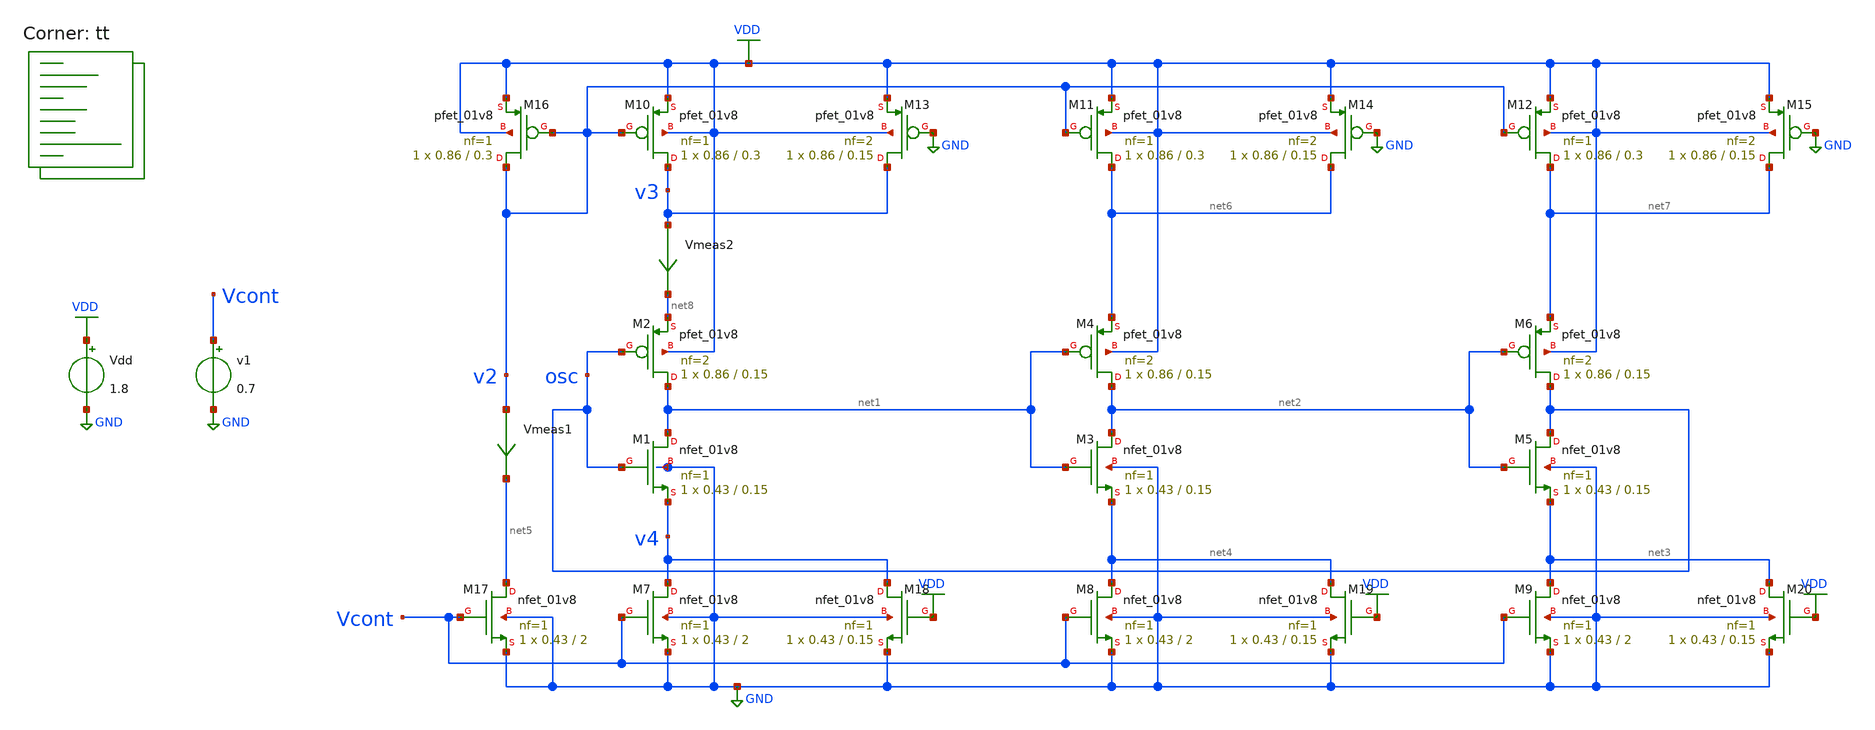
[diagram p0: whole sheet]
** sch_path: projects/pll/vco/xschem_ngspice/tb_current_starved_VCO4_4.sch
**.subckt tb_current_starved_VCO4_4
Vdd VDD GND 1.8
v1 Vcont GND 0.7
XM1 net1 osc v4 GND sky130_fd_pr__nfet_01v8 L=0.15 W=0.43 nf=1 ad='int((nf+1)/2) * W/nf * 0.29' as='int((nf+2)/2) * W/nf * 0.29'
+ pd='2*int((nf+1)/2) * (W/nf + 0.29)' ps='2*int((nf+2)/2) * (W/nf + 0.29)' nrd='0.29 / W' nrs='0.29 / W'
+ sa=0 sb=0 sd=0 mult=1 m=1
XM2 net1 osc net8 VDD sky130_fd_pr__pfet_01v8 L=0.15 W=0.86 nf=2 ad='int((nf+1)/2) * W/nf * 0.29' as='int((nf+2)/2) * W/nf * 0.29'
+ pd='2*int((nf+1)/2) * (W/nf + 0.29)' ps='2*int((nf+2)/2) * (W/nf + 0.29)' nrd='0.29 / W' nrs='0.29 / W'
+ sa=0 sb=0 sd=0 mult=1 m=1
XM3 net2 net1 net4 GND sky130_fd_pr__nfet_01v8 L=0.15 W=0.43 nf=1 ad='int((nf+1)/2) * W/nf * 0.29' as='int((nf+2)/2) * W/nf * 0.29'
+ pd='2*int((nf+1)/2) * (W/nf + 0.29)' ps='2*int((nf+2)/2) * (W/nf + 0.29)' nrd='0.29 / W' nrs='0.29 / W'
+ sa=0 sb=0 sd=0 mult=1 m=1
XM4 net2 net1 net6 VDD sky130_fd_pr__pfet_01v8 L=0.15 W=0.86 nf=2 ad='int((nf+1)/2) * W/nf * 0.29' as='int((nf+2)/2) * W/nf * 0.29'
+ pd='2*int((nf+1)/2) * (W/nf + 0.29)' ps='2*int((nf+2)/2) * (W/nf + 0.29)' nrd='0.29 / W' nrs='0.29 / W'
+ sa=0 sb=0 sd=0 mult=1 m=1
XM5 osc net2 net3 GND sky130_fd_pr__nfet_01v8 L=0.15 W=0.43 nf=1 ad='int((nf+1)/2) * W/nf * 0.29' as='int((nf+2)/2) * W/nf * 0.29'
+ pd='2*int((nf+1)/2) * (W/nf + 0.29)' ps='2*int((nf+2)/2) * (W/nf + 0.29)' nrd='0.29 / W' nrs='0.29 / W'
+ sa=0 sb=0 sd=0 mult=1 m=1
XM6 osc net2 net7 VDD sky130_fd_pr__pfet_01v8 L=0.15 W=0.86 nf=2 ad='int((nf+1)/2) * W/nf * 0.29' as='int((nf+2)/2) * W/nf * 0.29'
+ pd='2*int((nf+1)/2) * (W/nf + 0.29)' ps='2*int((nf+2)/2) * (W/nf + 0.29)' nrd='0.29 / W' nrs='0.29 / W'
+ sa=0 sb=0 sd=0 mult=1 m=1
XM7 v4 Vcont GND GND sky130_fd_pr__nfet_01v8 L=2 W=0.43 nf=1 ad='int((nf+1)/2) * W/nf * 0.29' as='int((nf+2)/2) * W/nf * 0.29'
+ pd='2*int((nf+1)/2) * (W/nf + 0.29)' ps='2*int((nf+2)/2) * (W/nf + 0.29)' nrd='0.29 / W' nrs='0.29 / W'
+ sa=0 sb=0 sd=0 mult=1 m=1
XM8 net4 Vcont GND GND sky130_fd_pr__nfet_01v8 L=2 W=0.43 nf=1 ad='int((nf+1)/2) * W/nf * 0.29' as='int((nf+2)/2) * W/nf * 0.29'
+ pd='2*int((nf+1)/2) * (W/nf + 0.29)' ps='2*int((nf+2)/2) * (W/nf + 0.29)' nrd='0.29 / W' nrs='0.29 / W'
+ sa=0 sb=0 sd=0 mult=1 m=1
XM9 net3 Vcont GND GND sky130_fd_pr__nfet_01v8 L=2 W=0.43 nf=1 ad='int((nf+1)/2) * W/nf * 0.29' as='int((nf+2)/2) * W/nf * 0.29'
+ pd='2*int((nf+1)/2) * (W/nf + 0.29)' ps='2*int((nf+2)/2) * (W/nf + 0.29)' nrd='0.29 / W' nrs='0.29 / W'
+ sa=0 sb=0 sd=0 mult=1 m=1
XM10 v3 v2 VDD VDD sky130_fd_pr__pfet_01v8 L=0.3 W=0.86 nf=1 ad='int((nf+1)/2) * W/nf * 0.29' as='int((nf+2)/2) * W/nf * 0.29'
+ pd='2*int((nf+1)/2) * (W/nf + 0.29)' ps='2*int((nf+2)/2) * (W/nf + 0.29)' nrd='0.29 / W' nrs='0.29 / W'
+ sa=0 sb=0 sd=0 mult=1 m=1
XM11 net6 v2 VDD VDD sky130_fd_pr__pfet_01v8 L=0.3 W=0.86 nf=1 ad='int((nf+1)/2) * W/nf * 0.29' as='int((nf+2)/2) * W/nf * 0.29'
+ pd='2*int((nf+1)/2) * (W/nf + 0.29)' ps='2*int((nf+2)/2) * (W/nf + 0.29)' nrd='0.29 / W' nrs='0.29 / W'
+ sa=0 sb=0 sd=0 mult=1 m=1
XM12 net7 v2 VDD VDD sky130_fd_pr__pfet_01v8 L=0.3 W=0.86 nf=1 ad='int((nf+1)/2) * W/nf * 0.29' as='int((nf+2)/2) * W/nf * 0.29'
+ pd='2*int((nf+1)/2) * (W/nf + 0.29)' ps='2*int((nf+2)/2) * (W/nf + 0.29)' nrd='0.29 / W' nrs='0.29 / W'
+ sa=0 sb=0 sd=0 mult=1 m=1
XM16 v2 v2 VDD VDD sky130_fd_pr__pfet_01v8 L=0.3 W=0.86 nf=1 ad='int((nf+1)/2) * W/nf * 0.29' as='int((nf+2)/2) * W/nf * 0.29'
+ pd='2*int((nf+1)/2) * (W/nf + 0.29)' ps='2*int((nf+2)/2) * (W/nf + 0.29)' nrd='0.29 / W' nrs='0.29 / W'
+ sa=0 sb=0 sd=0 mult=1 m=1
XM17 net5 Vcont GND GND sky130_fd_pr__nfet_01v8 L=2 W=0.43 nf=1 ad='int((nf+1)/2) * W/nf * 0.29' as='int((nf+2)/2) * W/nf * 0.29'
+ pd='2*int((nf+1)/2) * (W/nf + 0.29)' ps='2*int((nf+2)/2) * (W/nf + 0.29)' nrd='0.29 / W' nrs='0.29 / W'
+ sa=0 sb=0 sd=0 mult=1 m=1
Vmeas1 v2 net5 0
.save i(vmeas1)
XM13 v3 GND VDD VDD sky130_fd_pr__pfet_01v8 L=0.15 W=0.86 nf=2 ad='int((nf+1)/2) * W/nf * 0.29' as='int((nf+2)/2) * W/nf * 0.29'
+ pd='2*int((nf+1)/2) * (W/nf + 0.29)' ps='2*int((nf+2)/2) * (W/nf + 0.29)' nrd='0.29 / W' nrs='0.29 / W'
+ sa=0 sb=0 sd=0 mult=1 m=1
XM14 net6 GND VDD VDD sky130_fd_pr__pfet_01v8 L=0.15 W=0.86 nf=2 ad='int((nf+1)/2) * W/nf * 0.29' as='int((nf+2)/2) * W/nf * 0.29'
+ pd='2*int((nf+1)/2) * (W/nf + 0.29)' ps='2*int((nf+2)/2) * (W/nf + 0.29)' nrd='0.29 / W' nrs='0.29 / W'
+ sa=0 sb=0 sd=0 mult=1 m=1
XM15 net7 GND VDD VDD sky130_fd_pr__pfet_01v8 L=0.15 W=0.86 nf=2 ad='int((nf+1)/2) * W/nf * 0.29' as='int((nf+2)/2) * W/nf * 0.29'
+ pd='2*int((nf+1)/2) * (W/nf + 0.29)' ps='2*int((nf+2)/2) * (W/nf + 0.29)' nrd='0.29 / W' nrs='0.29 / W'
+ sa=0 sb=0 sd=0 mult=1 m=1
XM18 v4 VDD GND GND sky130_fd_pr__nfet_01v8 L=0.15 W=0.43 nf=1 ad='int((nf+1)/2) * W/nf * 0.29' as='int((nf+2)/2) * W/nf * 0.29'
+ pd='2*int((nf+1)/2) * (W/nf + 0.29)' ps='2*int((nf+2)/2) * (W/nf + 0.29)' nrd='0.29 / W' nrs='0.29 / W'
+ sa=0 sb=0 sd=0 mult=1 m=1
XM19 net4 VDD GND GND sky130_fd_pr__nfet_01v8 L=0.15 W=0.43 nf=1 ad='int((nf+1)/2) * W/nf * 0.29' as='int((nf+2)/2) * W/nf * 0.29'
+ pd='2*int((nf+1)/2) * (W/nf + 0.29)' ps='2*int((nf+2)/2) * (W/nf + 0.29)' nrd='0.29 / W' nrs='0.29 / W'
+ sa=0 sb=0 sd=0 mult=1 m=1
XM20 net3 VDD GND GND sky130_fd_pr__nfet_01v8 L=0.15 W=0.43 nf=1 ad='int((nf+1)/2) * W/nf * 0.29' as='int((nf+2)/2) * W/nf * 0.29'
+ pd='2*int((nf+1)/2) * (W/nf + 0.29)' ps='2*int((nf+2)/2) * (W/nf + 0.29)' nrd='0.29 / W' nrs='0.29 / W'
+ sa=0 sb=0 sd=0 mult=1 m=1
Vmeas2 v3 net8 0
.save i(vmeas2)
**** begin user architecture code
.lib $::SKYWATER_MODELS/sky130.lib.spice tt



* .option method=gear
.option method=trap
.option wnflag=1


*.ic v(vcont)=1.2

* .temp = 75

.control

  let v_cont_start = 0.0
  * let v_cont_start = 1.1
  * let v_cont_stop = 1.32
  let v_cont_stop = 1.9

  dowhile v_cont_start <= v_cont_stop
    alter v1 $&v_cont_start
    save v(vcont) v(osc) v(vout) v(v1) v(v2) v(v3) v(v4) i(vmeas) i(vmeas1)
    * save all
    tran 2ps 30ns
    remzerovec
    write tb_current_starved_VCO4_4_{$&v_cont_start}.raw
    * write tb_current_starved_VCO4_4_.raw
    linearize v(osc)
    let filename = v_cont_start * 100
    wrdata /foss/designs/my_design/projects/pll/vco/xschem_ngspice/tb_current_starved_VCO4_4_{$&filename}.txt
+ v(osc)
    set appendwrite

    reset
    let v_cont_start = v_cont_start + 0.1
  end
.endc




**** end user architecture code
**.ends
.GLOBAL GND
.GLOBAL VDD
.end
